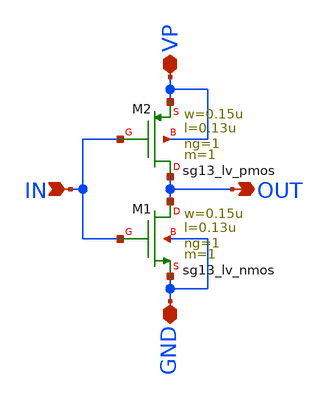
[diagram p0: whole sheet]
** sch_path: schematics/divider/schematics/inverter_dek.sch
**.subckt inverter_dek IN VP OUT GND
*.ipin IN
*.iopin VP
*.opin OUT
*.iopin GND
XM1 OUT IN GND GND sg13_lv_nmos w=0.15u l=0.13u ng=1 m=1 mm_ok=1
XM2 OUT IN VP VP sg13_lv_pmos w=0.15u l=0.13u ng=1 m=1 mm_ok=1
**.ends
.end
